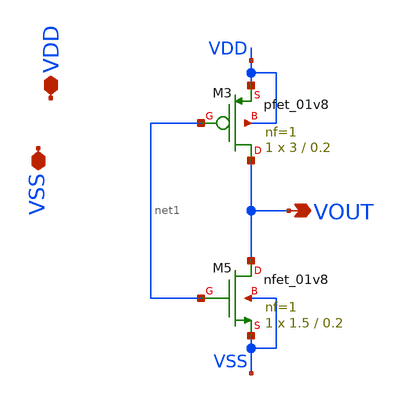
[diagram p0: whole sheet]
** sch_path: Xschem/PLL_TOP_Schematics/untitled-1.sch
**.subckt untitled-1 VOUT VSS VDD
*.opin VOUT
*.iopin VSS
*.iopin VDD
XM3 VOUT net1 VDD VDD sky130_fd_pr__pfet_01v8 L=0.2 W=3 nf=1 ad='int((nf+1)/2) * W/nf * 0.29' as='int((nf+2)/2) * W/nf * 0.29'
+ pd='2*int((nf+1)/2) * (W/nf + 0.29)' ps='2*int((nf+2)/2) * (W/nf + 0.29)' nrd='0.29 / W' nrs='0.29 / W'
+ sa=0 sb=0 sd=0 mult=1 m=1
XM5 VOUT net1 VSS VSS sky130_fd_pr__nfet_01v8 L=0.2 W=1.5 nf=1 ad='int((nf+1)/2) * W/nf * 0.29' as='int((nf+2)/2) * W/nf * 0.29'
+ pd='2*int((nf+1)/2) * (W/nf + 0.29)' ps='2*int((nf+2)/2) * (W/nf + 0.29)' nrd='0.29 / W' nrs='0.29 / W'
+ sa=0 sb=0 sd=0 mult=1 m=1
**.ends
.end
